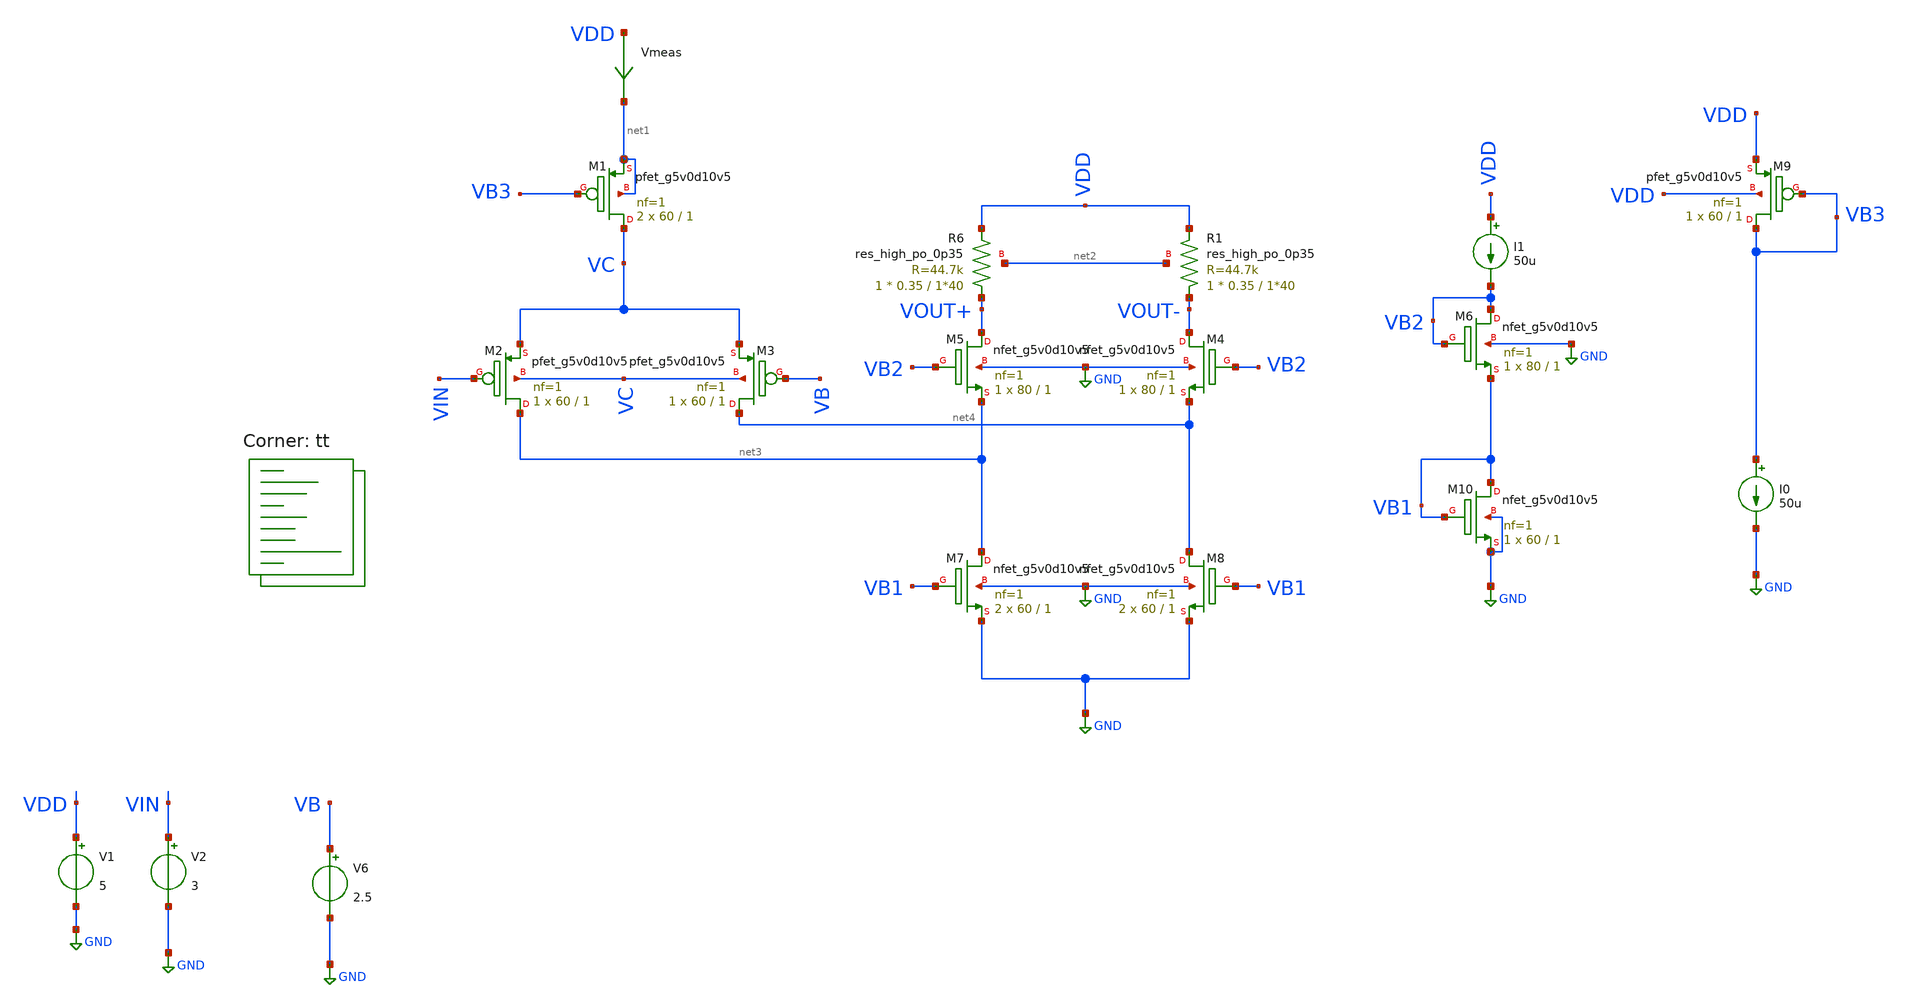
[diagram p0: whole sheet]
** sch_path: amplifiers/differencial_stage_amps/basic_stages/folded_cascode/diferential_stage.sch
**.subckt diferential_stage
V1 VDD GND 5
V2 VIN GND 3
V6 VB GND 2.5
I0 VB3 GND 50u
Vmeas VDD net1 0
.save i(vmeas)
XM9 VB3 VB3 VDD VDD sky130_fd_pr__pfet_g5v0d10v5 L=1 W=60 nf=1 ad='int((1 + 1)/2) * 60 / 1 * 0.29' as='int((1 + 2)/2) * 60 / 1 * 0.29'
+ pd='2*int((1 + 1)/2) * (60 / 1 + 0.29)' ps='2*int((1 + 2)/2) * (60 / 1 + 0.29)' nrd='0.29 / 60 ' nrs='0.29 / 60 '
+ sa=0 sb=0 sd=0 mult=1 m=1
XM1 VC VB3 net1 net1 sky130_fd_pr__pfet_g5v0d10v5 L=1 W=60 nf=1 ad='int((1 + 1)/2) * 60 / 1 * 0.29' as='int((1 + 2)/2) * 60 / 1 * 0.29'
+ pd='2*int((1 + 1)/2) * (60 / 1 + 0.29)' ps='2*int((1 + 2)/2) * (60 / 1 + 0.29)' nrd='0.29 / 60 ' nrs='0.29 / 60 '
+ sa=0 sb=0 sd=0 mult=2 m=2
XM2 net3 VIN VC VC sky130_fd_pr__pfet_g5v0d10v5 L=1 W=60 nf=1 ad='int((1 + 1)/2) * 60 / 1 * 0.29' as='int((1 + 2)/2) * 60 / 1 * 0.29'
+ pd='2*int((1 + 1)/2) * (60 / 1 + 0.29)' ps='2*int((1 + 2)/2) * (60 / 1 + 0.29)' nrd='0.29 / 60 ' nrs='0.29 / 60 '
+ sa=0 sb=0 sd=0 mult=1 m=1
XM3 net4 VB VC VC sky130_fd_pr__pfet_g5v0d10v5 L=1 W=60 nf=1 ad='int((1 + 1)/2) * 60 / 1 * 0.29' as='int((1 + 2)/2) * 60 / 1 * 0.29'
+ pd='2*int((1 + 1)/2) * (60 / 1 + 0.29)' ps='2*int((1 + 2)/2) * (60 / 1 + 0.29)' nrd='0.29 / 60 ' nrs='0.29 / 60 '
+ sa=0 sb=0 sd=0 mult=1 m=1
XR6 VOUT+ VDD net2 sky130_fd_pr__res_high_po_0p35 L=1*40 mult=1 m=1
XR1 VOUT- VDD net2 sky130_fd_pr__res_high_po_0p35 L=1*40 mult=1 m=1
XM5 VOUT+ VB2 net3 GND sky130_fd_pr__nfet_g5v0d10v5 L=1 W=80 nf=1 ad='int((1 + 1)/2) * 80 / 1 * 0.29'
+ as='int((1 + 2)/2) * 80 / 1 * 0.29' pd='2*int((1 + 1)/2) * (80 / 1 + 0.29)' ps='2*int((1 + 2)/2) * (80 / 1 + 0.29)'
+ nrd='0.29 / 80 ' nrs='0.29 / 80 ' sa=0 sb=0 sd=0 mult=1 m=1
XM4 VOUT- VB2 net4 GND sky130_fd_pr__nfet_g5v0d10v5 L=1 W=80 nf=1 ad='int((1 + 1)/2) * 80 / 1 * 0.29'
+ as='int((1 + 2)/2) * 80 / 1 * 0.29' pd='2*int((1 + 1)/2) * (80 / 1 + 0.29)' ps='2*int((1 + 2)/2) * (80 / 1 + 0.29)'
+ nrd='0.29 / 80 ' nrs='0.29 / 80 ' sa=0 sb=0 sd=0 mult=1 m=1
I1 VDD VB2 50u
XM6 VB2 VB2 VB1 GND sky130_fd_pr__nfet_g5v0d10v5 L=1 W=80 nf=1 ad='int((1 + 1)/2) * 80 / 1 * 0.29' as='int((1 + 2)/2) * 80 / 1 * 0.29'
+ pd='2*int((1 + 1)/2) * (80 / 1 + 0.29)' ps='2*int((1 + 2)/2) * (80 / 1 + 0.29)' nrd='0.29 / 80 ' nrs='0.29 / 80 '
+ sa=0 sb=0 sd=0 mult=1 m=1
XM7 net3 VB1 GND GND sky130_fd_pr__nfet_g5v0d10v5 L=1 W=60 nf=1 ad='int((1 + 1)/2) * 60 / 1 * 0.29' as='int((1 + 2)/2) * 60 / 1 * 0.29'
+ pd='2*int((1 + 1)/2) * (60 / 1 + 0.29)' ps='2*int((1 + 2)/2) * (60 / 1 + 0.29)' nrd='0.29 / 60 ' nrs='0.29 / 60 '
+ sa=0 sb=0 sd=0 mult=2 m=2
XM8 net4 VB1 GND GND sky130_fd_pr__nfet_g5v0d10v5 L=1 W=60 nf=1 ad='int((1 + 1)/2) * 60 / 1 * 0.29' as='int((1 + 2)/2) * 60 / 1 * 0.29'
+ pd='2*int((1 + 1)/2) * (60 / 1 + 0.29)' ps='2*int((1 + 2)/2) * (60 / 1 + 0.29)' nrd='0.29 / 60 ' nrs='0.29 / 60 '
+ sa=0 sb=0 sd=0 mult=2 m=2
XM10 VB1 VB1 GND GND sky130_fd_pr__nfet_g5v0d10v5 L=1 W=60 nf=1 ad='int((1 + 1)/2) * 60 / 1 * 0.29' as='int((1 + 2)/2) * 60 / 1 * 0.29'
+ pd='2*int((1 + 1)/2) * (60 / 1 + 0.29)' ps='2*int((1 + 2)/2) * (60 / 1 + 0.29)' nrd='0.29 / 60 ' nrs='0.29 / 60 '
+ sa=0 sb=0 sd=0 mult=1 m=1
**** begin user architecture code

**************************************************************
**************************************************************
**************************************************************
**************************************************************
**************************************************************
*LIBs*********************************************************
**************************************************************
**************************************************************
**************************************************************
**************************************************************
**************************************************************
*.lib $::SKYWATER_MODELS/sky130.lib.spice tt
* chose the corners in the corner file
* tt_mm for mismatch
* ss ff sf fs standart corners
* ll hh lh hl capacitor and resistors corners
* mc for total process variation including corners
**************************************************************
**************************************************************
**************************************************************
**************************************************************
**************************************************************
*Corners/montecarlo options***********************************
**************************************************************
**************************************************************
**************************************************************
**************************************************************
**************************************************************
.TEMP 27
**************************************************************
**************************************************************
**************************************************************
**************************************************************
*SIMULATION and Plots*****************************************
**************************************************************
**************************************************************
**************************************************************
**************************************************************
.control
save all
dc V2 0 5 0.01
*dc simulation
plot v(VOUT+) deriv(v(VOUT+))
plot i(Vmeas)

.endc

.lib $::SKYWATER_MODELS/sky130.lib.spice tt
**** end user architecture code
**.ends
.GLOBAL GND
.end
